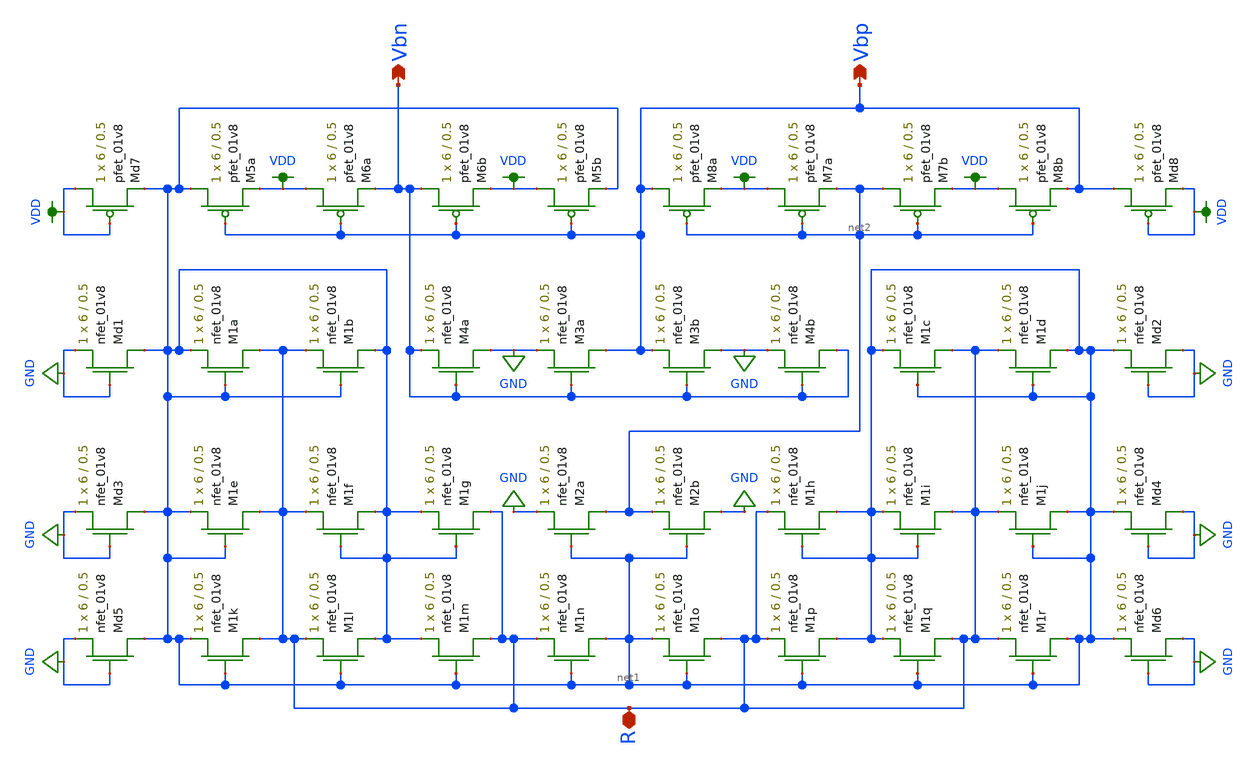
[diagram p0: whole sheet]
** sch_path: schematics/bias/current_bias_layout_driven.sch
**.subckt current_bias_layout_driven Vbn Vbp R
*.opin Vbn
*.opin Vbp
*.iopin R
XM5a net1 Vbp VDD VDD sky130_fd_pr__pfet_01v8 L=0.5 W=6 nf=1 ad='int((nf+1)/2) * W/nf * 0.29' as='int((nf+2)/2) * W/nf * 0.29'
+ pd='2*int((nf+1)/2) * (W/nf + 0.29)' ps='2*int((nf+2)/2) * (W/nf + 0.29)' nrd='0.29 / W' nrs='0.29 / W'
+ sa=0 sb=0 sd=0 mult=1 m=1
XM5b VDD Vbp net1 VDD sky130_fd_pr__pfet_01v8 L=0.5 W=6 nf=1 ad='int((nf+1)/2) * W/nf * 0.29' as='int((nf+2)/2) * W/nf * 0.29'
+ pd='2*int((nf+1)/2) * (W/nf + 0.29)' ps='2*int((nf+2)/2) * (W/nf + 0.29)' nrd='0.29 / W' nrs='0.29 / W'
+ sa=0 sb=0 sd=0 mult=1 m=1
XM1i R net1 net1 GND sky130_fd_pr__nfet_01v8 L=0.5 W=6 nf=1 ad='int((nf+1)/2) * W/nf * 0.29' as='int((nf+2)/2) * W/nf * 0.29'
+ pd='2*int((nf+1)/2) * (W/nf + 0.29)' ps='2*int((nf+2)/2) * (W/nf + 0.29)' nrd='0.29 / W' nrs='0.29 / W'
+ sa=0 sb=0 sd=0 mult=1 m=1
XM1h net1 net1 R GND sky130_fd_pr__nfet_01v8 L=0.5 W=6 nf=1 ad='int((nf+1)/2) * W/nf * 0.29' as='int((nf+2)/2) * W/nf * 0.29'
+ pd='2*int((nf+1)/2) * (W/nf + 0.29)' ps='2*int((nf+2)/2) * (W/nf + 0.29)' nrd='0.29 / W' nrs='0.29 / W'
+ sa=0 sb=0 sd=0 mult=1 m=1
XM1g R net1 net1 GND sky130_fd_pr__nfet_01v8 L=0.5 W=6 nf=1 ad='int((nf+1)/2) * W/nf * 0.29' as='int((nf+2)/2) * W/nf * 0.29'
+ pd='2*int((nf+1)/2) * (W/nf + 0.29)' ps='2*int((nf+2)/2) * (W/nf + 0.29)' nrd='0.29 / W' nrs='0.29 / W'
+ sa=0 sb=0 sd=0 mult=1 m=1
XM1f net1 net1 R GND sky130_fd_pr__nfet_01v8 L=0.5 W=6 nf=1 ad='int((nf+1)/2) * W/nf * 0.29' as='int((nf+2)/2) * W/nf * 0.29'
+ pd='2*int((nf+1)/2) * (W/nf + 0.29)' ps='2*int((nf+2)/2) * (W/nf + 0.29)' nrd='0.29 / W' nrs='0.29 / W'
+ sa=0 sb=0 sd=0 mult=1 m=1
XM1e R net1 net1 GND sky130_fd_pr__nfet_01v8 L=0.5 W=6 nf=1 ad='int((nf+1)/2) * W/nf * 0.29' as='int((nf+2)/2) * W/nf * 0.29'
+ pd='2*int((nf+1)/2) * (W/nf + 0.29)' ps='2*int((nf+2)/2) * (W/nf + 0.29)' nrd='0.29 / W' nrs='0.29 / W'
+ sa=0 sb=0 sd=0 mult=1 m=1
XM1d net1 net1 R GND sky130_fd_pr__nfet_01v8 L=0.5 W=6 nf=1 ad='int((nf+1)/2) * W/nf * 0.29' as='int((nf+2)/2) * W/nf * 0.29'
+ pd='2*int((nf+1)/2) * (W/nf + 0.29)' ps='2*int((nf+2)/2) * (W/nf + 0.29)' nrd='0.29 / W' nrs='0.29 / W'
+ sa=0 sb=0 sd=0 mult=1 m=1
XM1c R net1 net1 GND sky130_fd_pr__nfet_01v8 L=0.5 W=6 nf=1 ad='int((nf+1)/2) * W/nf * 0.29' as='int((nf+2)/2) * W/nf * 0.29'
+ pd='2*int((nf+1)/2) * (W/nf + 0.29)' ps='2*int((nf+2)/2) * (W/nf + 0.29)' nrd='0.29 / W' nrs='0.29 / W'
+ sa=0 sb=0 sd=0 mult=1 m=1
XM1b net1 net1 R GND sky130_fd_pr__nfet_01v8 L=0.5 W=6 nf=1 ad='int((nf+1)/2) * W/nf * 0.29' as='int((nf+2)/2) * W/nf * 0.29'
+ pd='2*int((nf+1)/2) * (W/nf + 0.29)' ps='2*int((nf+2)/2) * (W/nf + 0.29)' nrd='0.29 / W' nrs='0.29 / W'
+ sa=0 sb=0 sd=0 mult=1 m=1
XM1a R net1 net1 GND sky130_fd_pr__nfet_01v8 L=0.5 W=6 nf=1 ad='int((nf+1)/2) * W/nf * 0.29' as='int((nf+2)/2) * W/nf * 0.29'
+ pd='2*int((nf+1)/2) * (W/nf + 0.29)' ps='2*int((nf+2)/2) * (W/nf + 0.29)' nrd='0.29 / W' nrs='0.29 / W'
+ sa=0 sb=0 sd=0 mult=1 m=1
XM7a VDD net2 net2 VDD sky130_fd_pr__pfet_01v8 L=0.5 W=6 nf=1 ad='int((nf+1)/2) * W/nf * 0.29' as='int((nf+2)/2) * W/nf * 0.29'
+ pd='2*int((nf+1)/2) * (W/nf + 0.29)' ps='2*int((nf+2)/2) * (W/nf + 0.29)' nrd='0.29 / W' nrs='0.29 / W'
+ sa=0 sb=0 sd=0 mult=1 m=1
XM7b net2 net2 VDD VDD sky130_fd_pr__pfet_01v8 L=0.5 W=6 nf=1 ad='int((nf+1)/2) * W/nf * 0.29' as='int((nf+2)/2) * W/nf * 0.29'
+ pd='2*int((nf+1)/2) * (W/nf + 0.29)' ps='2*int((nf+2)/2) * (W/nf + 0.29)' nrd='0.29 / W' nrs='0.29 / W'
+ sa=0 sb=0 sd=0 mult=1 m=1
XM8b VDD net2 Vbp VDD sky130_fd_pr__pfet_01v8 L=0.5 W=6 nf=1 ad='int((nf+1)/2) * W/nf * 0.29' as='int((nf+2)/2) * W/nf * 0.29'
+ pd='2*int((nf+1)/2) * (W/nf + 0.29)' ps='2*int((nf+2)/2) * (W/nf + 0.29)' nrd='0.29 / W' nrs='0.29 / W'
+ sa=0 sb=0 sd=0 mult=1 m=1
XM8a Vbp net2 VDD VDD sky130_fd_pr__pfet_01v8 L=0.5 W=6 nf=1 ad='int((nf+1)/2) * W/nf * 0.29' as='int((nf+2)/2) * W/nf * 0.29'
+ pd='2*int((nf+1)/2) * (W/nf + 0.29)' ps='2*int((nf+2)/2) * (W/nf + 0.29)' nrd='0.29 / W' nrs='0.29 / W'
+ sa=0 sb=0 sd=0 mult=1 m=1
XM6b Vbn Vbp VDD VDD sky130_fd_pr__pfet_01v8 L=0.5 W=6 nf=1 ad='int((nf+1)/2) * W/nf * 0.29' as='int((nf+2)/2) * W/nf * 0.29'
+ pd='2*int((nf+1)/2) * (W/nf + 0.29)' ps='2*int((nf+2)/2) * (W/nf + 0.29)' nrd='0.29 / W' nrs='0.29 / W'
+ sa=0 sb=0 sd=0 mult=1 m=1
XM6a VDD Vbp Vbn VDD sky130_fd_pr__pfet_01v8 L=0.5 W=6 nf=1 ad='int((nf+1)/2) * W/nf * 0.29' as='int((nf+2)/2) * W/nf * 0.29'
+ pd='2*int((nf+1)/2) * (W/nf + 0.29)' ps='2*int((nf+2)/2) * (W/nf + 0.29)' nrd='0.29 / W' nrs='0.29 / W'
+ sa=0 sb=0 sd=0 mult=1 m=1
XM2a net2 net1 GND GND sky130_fd_pr__nfet_01v8 L=0.5 W=6 nf=1 ad='int((nf+1)/2) * W/nf * 0.29' as='int((nf+2)/2) * W/nf * 0.29'
+ pd='2*int((nf+1)/2) * (W/nf + 0.29)' ps='2*int((nf+2)/2) * (W/nf + 0.29)' nrd='0.29 / W' nrs='0.29 / W'
+ sa=0 sb=0 sd=0 mult=1 m=1
XM2b GND net1 net2 GND sky130_fd_pr__nfet_01v8 L=0.5 W=6 nf=1 ad='int((nf+1)/2) * W/nf * 0.29' as='int((nf+2)/2) * W/nf * 0.29'
+ pd='2*int((nf+1)/2) * (W/nf + 0.29)' ps='2*int((nf+2)/2) * (W/nf + 0.29)' nrd='0.29 / W' nrs='0.29 / W'
+ sa=0 sb=0 sd=0 mult=1 m=1
XM3b GND Vbn Vbp GND sky130_fd_pr__nfet_01v8 L=0.5 W=6 nf=1 ad='int((nf+1)/2) * W/nf * 0.29' as='int((nf+2)/2) * W/nf * 0.29'
+ pd='2*int((nf+1)/2) * (W/nf + 0.29)' ps='2*int((nf+2)/2) * (W/nf + 0.29)' nrd='0.29 / W' nrs='0.29 / W'
+ sa=0 sb=0 sd=0 mult=1 m=1
XM3a Vbp Vbn GND GND sky130_fd_pr__nfet_01v8 L=0.5 W=6 nf=1 ad='int((nf+1)/2) * W/nf * 0.29' as='int((nf+2)/2) * W/nf * 0.29'
+ pd='2*int((nf+1)/2) * (W/nf + 0.29)' ps='2*int((nf+2)/2) * (W/nf + 0.29)' nrd='0.29 / W' nrs='0.29 / W'
+ sa=0 sb=0 sd=0 mult=1 m=1
XM4a GND Vbn Vbn GND sky130_fd_pr__nfet_01v8 L=0.5 W=6 nf=1 ad='int((nf+1)/2) * W/nf * 0.29' as='int((nf+2)/2) * W/nf * 0.29'
+ pd='2*int((nf+1)/2) * (W/nf + 0.29)' ps='2*int((nf+2)/2) * (W/nf + 0.29)' nrd='0.29 / W' nrs='0.29 / W'
+ sa=0 sb=0 sd=0 mult=1 m=1
XM4b Vbn Vbn GND GND sky130_fd_pr__nfet_01v8 L=0.5 W=6 nf=1 ad='int((nf+1)/2) * W/nf * 0.29' as='int((nf+2)/2) * W/nf * 0.29'
+ pd='2*int((nf+1)/2) * (W/nf + 0.29)' ps='2*int((nf+2)/2) * (W/nf + 0.29)' nrd='0.29 / W' nrs='0.29 / W'
+ sa=0 sb=0 sd=0 mult=1 m=1
XM1r net1 net1 R GND sky130_fd_pr__nfet_01v8 L=0.5 W=6 nf=1 ad='int((nf+1)/2) * W/nf * 0.29' as='int((nf+2)/2) * W/nf * 0.29'
+ pd='2*int((nf+1)/2) * (W/nf + 0.29)' ps='2*int((nf+2)/2) * (W/nf + 0.29)' nrd='0.29 / W' nrs='0.29 / W'
+ sa=0 sb=0 sd=0 mult=1 m=1
XM1q R net1 net1 GND sky130_fd_pr__nfet_01v8 L=0.5 W=6 nf=1 ad='int((nf+1)/2) * W/nf * 0.29' as='int((nf+2)/2) * W/nf * 0.29'
+ pd='2*int((nf+1)/2) * (W/nf + 0.29)' ps='2*int((nf+2)/2) * (W/nf + 0.29)' nrd='0.29 / W' nrs='0.29 / W'
+ sa=0 sb=0 sd=0 mult=1 m=1
XM1p net1 net1 R GND sky130_fd_pr__nfet_01v8 L=0.5 W=6 nf=1 ad='int((nf+1)/2) * W/nf * 0.29' as='int((nf+2)/2) * W/nf * 0.29'
+ pd='2*int((nf+1)/2) * (W/nf + 0.29)' ps='2*int((nf+2)/2) * (W/nf + 0.29)' nrd='0.29 / W' nrs='0.29 / W'
+ sa=0 sb=0 sd=0 mult=1 m=1
XM1o R net1 net1 GND sky130_fd_pr__nfet_01v8 L=0.5 W=6 nf=1 ad='int((nf+1)/2) * W/nf * 0.29' as='int((nf+2)/2) * W/nf * 0.29'
+ pd='2*int((nf+1)/2) * (W/nf + 0.29)' ps='2*int((nf+2)/2) * (W/nf + 0.29)' nrd='0.29 / W' nrs='0.29 / W'
+ sa=0 sb=0 sd=0 mult=1 m=1
XM1n net1 net1 R GND sky130_fd_pr__nfet_01v8 L=0.5 W=6 nf=1 ad='int((nf+1)/2) * W/nf * 0.29' as='int((nf+2)/2) * W/nf * 0.29'
+ pd='2*int((nf+1)/2) * (W/nf + 0.29)' ps='2*int((nf+2)/2) * (W/nf + 0.29)' nrd='0.29 / W' nrs='0.29 / W'
+ sa=0 sb=0 sd=0 mult=1 m=1
XM1m R net1 net1 GND sky130_fd_pr__nfet_01v8 L=0.5 W=6 nf=1 ad='int((nf+1)/2) * W/nf * 0.29' as='int((nf+2)/2) * W/nf * 0.29'
+ pd='2*int((nf+1)/2) * (W/nf + 0.29)' ps='2*int((nf+2)/2) * (W/nf + 0.29)' nrd='0.29 / W' nrs='0.29 / W'
+ sa=0 sb=0 sd=0 mult=1 m=1
XM1l net1 net1 R GND sky130_fd_pr__nfet_01v8 L=0.5 W=6 nf=1 ad='int((nf+1)/2) * W/nf * 0.29' as='int((nf+2)/2) * W/nf * 0.29'
+ pd='2*int((nf+1)/2) * (W/nf + 0.29)' ps='2*int((nf+2)/2) * (W/nf + 0.29)' nrd='0.29 / W' nrs='0.29 / W'
+ sa=0 sb=0 sd=0 mult=1 m=1
XM1k R net1 net1 GND sky130_fd_pr__nfet_01v8 L=0.5 W=6 nf=1 ad='int((nf+1)/2) * W/nf * 0.29' as='int((nf+2)/2) * W/nf * 0.29'
+ pd='2*int((nf+1)/2) * (W/nf + 0.29)' ps='2*int((nf+2)/2) * (W/nf + 0.29)' nrd='0.29 / W' nrs='0.29 / W'
+ sa=0 sb=0 sd=0 mult=1 m=1
XM1j net1 net1 R GND sky130_fd_pr__nfet_01v8 L=0.5 W=6 nf=1 ad='int((nf+1)/2) * W/nf * 0.29' as='int((nf+2)/2) * W/nf * 0.29'
+ pd='2*int((nf+1)/2) * (W/nf + 0.29)' ps='2*int((nf+2)/2) * (W/nf + 0.29)' nrd='0.29 / W' nrs='0.29 / W'
+ sa=0 sb=0 sd=0 mult=1 m=1
XMd1 net1 GND GND GND sky130_fd_pr__nfet_01v8 L=0.5 W=6 nf=1 ad='int((nf+1)/2) * W/nf * 0.29' as='int((nf+2)/2) * W/nf * 0.29'
+ pd='2*int((nf+1)/2) * (W/nf + 0.29)' ps='2*int((nf+2)/2) * (W/nf + 0.29)' nrd='0.29 / W' nrs='0.29 / W'
+ sa=0 sb=0 sd=0 mult=1 m=1
XMd2 GND GND net1 GND sky130_fd_pr__nfet_01v8 L=0.5 W=6 nf=1 ad='int((nf+1)/2) * W/nf * 0.29' as='int((nf+2)/2) * W/nf * 0.29'
+ pd='2*int((nf+1)/2) * (W/nf + 0.29)' ps='2*int((nf+2)/2) * (W/nf + 0.29)' nrd='0.29 / W' nrs='0.29 / W'
+ sa=0 sb=0 sd=0 mult=1 m=1
XMd3 net1 GND GND GND sky130_fd_pr__nfet_01v8 L=0.5 W=6 nf=1 ad='int((nf+1)/2) * W/nf * 0.29' as='int((nf+2)/2) * W/nf * 0.29'
+ pd='2*int((nf+1)/2) * (W/nf + 0.29)' ps='2*int((nf+2)/2) * (W/nf + 0.29)' nrd='0.29 / W' nrs='0.29 / W'
+ sa=0 sb=0 sd=0 mult=1 m=1
XMd4 GND GND net1 GND sky130_fd_pr__nfet_01v8 L=0.5 W=6 nf=1 ad='int((nf+1)/2) * W/nf * 0.29' as='int((nf+2)/2) * W/nf * 0.29'
+ pd='2*int((nf+1)/2) * (W/nf + 0.29)' ps='2*int((nf+2)/2) * (W/nf + 0.29)' nrd='0.29 / W' nrs='0.29 / W'
+ sa=0 sb=0 sd=0 mult=1 m=1
XMd5 net1 GND GND GND sky130_fd_pr__nfet_01v8 L=0.5 W=6 nf=1 ad='int((nf+1)/2) * W/nf * 0.29' as='int((nf+2)/2) * W/nf * 0.29'
+ pd='2*int((nf+1)/2) * (W/nf + 0.29)' ps='2*int((nf+2)/2) * (W/nf + 0.29)' nrd='0.29 / W' nrs='0.29 / W'
+ sa=0 sb=0 sd=0 mult=1 m=1
XMd6 GND GND net1 GND sky130_fd_pr__nfet_01v8 L=0.5 W=6 nf=1 ad='int((nf+1)/2) * W/nf * 0.29' as='int((nf+2)/2) * W/nf * 0.29'
+ pd='2*int((nf+1)/2) * (W/nf + 0.29)' ps='2*int((nf+2)/2) * (W/nf + 0.29)' nrd='0.29 / W' nrs='0.29 / W'
+ sa=0 sb=0 sd=0 mult=1 m=1
XMd7 VDD VDD net1 VDD sky130_fd_pr__pfet_01v8 L=0.5 W=6 nf=1 ad='int((nf+1)/2) * W/nf * 0.29' as='int((nf+2)/2) * W/nf * 0.29'
+ pd='2*int((nf+1)/2) * (W/nf + 0.29)' ps='2*int((nf+2)/2) * (W/nf + 0.29)' nrd='0.29 / W' nrs='0.29 / W'
+ sa=0 sb=0 sd=0 mult=1 m=1
XMd8 Vbp VDD VDD VDD sky130_fd_pr__pfet_01v8 L=0.5 W=6 nf=1 ad='int((nf+1)/2) * W/nf * 0.29' as='int((nf+2)/2) * W/nf * 0.29'
+ pd='2*int((nf+1)/2) * (W/nf + 0.29)' ps='2*int((nf+2)/2) * (W/nf + 0.29)' nrd='0.29 / W' nrs='0.29 / W'
+ sa=0 sb=0 sd=0 mult=1 m=1
**.ends
.GLOBAL VDD
.GLOBAL GND
.end
